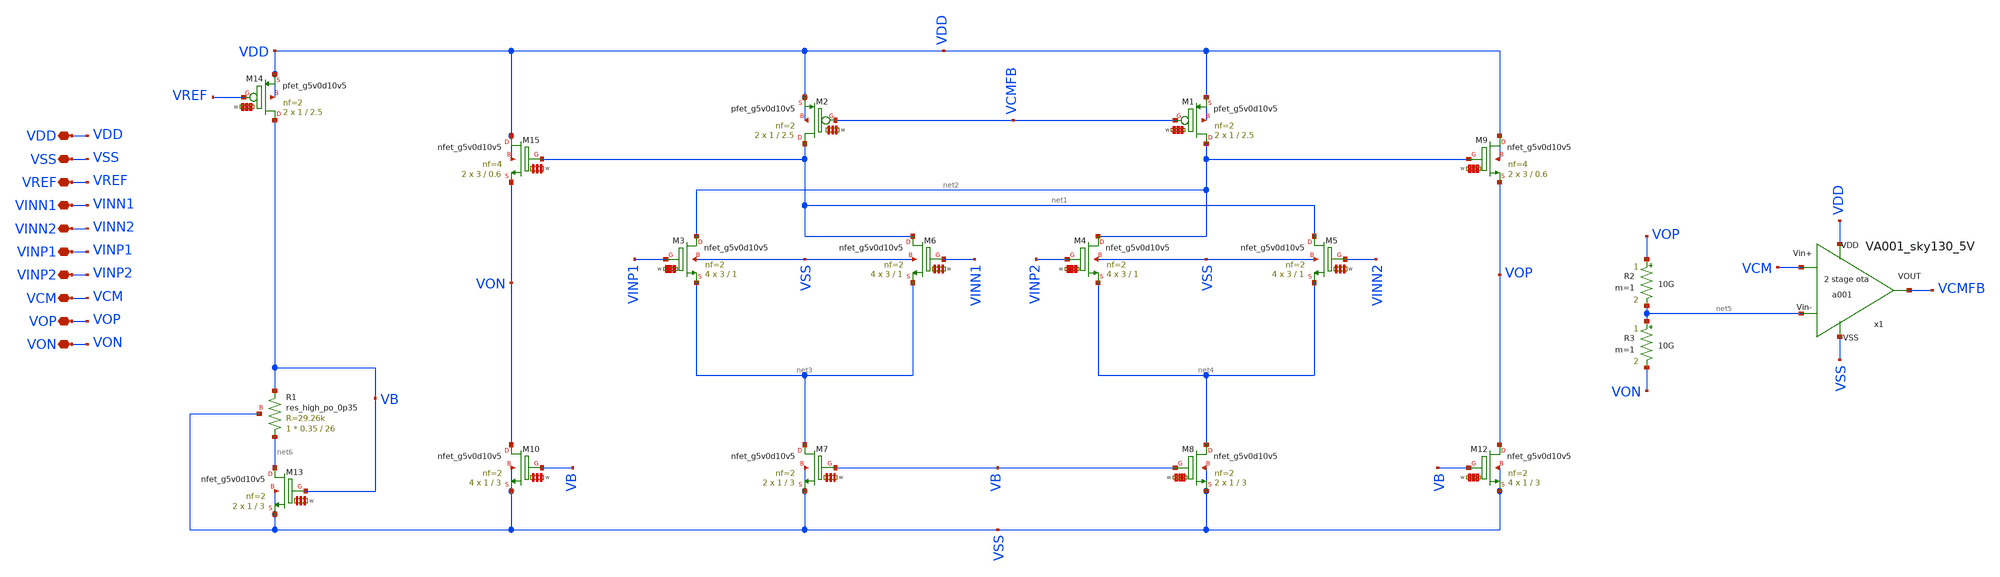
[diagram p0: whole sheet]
** sch_path: LIB/Sky130A/DDA/DDA002_NMOS_sky130_5V.sch
**.subckt DDA002_NMOS_sky130_5V VDD VSS VREF VINN1 VINN2 VINP1 VINP2 VCM VOP VON
*.iopin VDD
*.iopin VSS
*.iopin VREF
*.iopin VINN1
*.iopin VINN2
*.iopin VINP1
*.iopin VINP2
*.iopin VCM
*.iopin VOP
*.iopin VON
XM2 net1 VCMFB VDD VDD sky130_fd_pr__pfet_g5v0d10v5 L=2.5 W='1 * 2 ' nf=2 ad='int((2 + 1)/2) * 1 * 0.29'
+ as='int((2 + 2)/2) * 1 * 0.29' pd='2*int((2 + 1)/2) * (1 + 0.29)' ps='2*int((2 + 2)/2) * (1 + 0.29)'
+ nrd='0.29 / 1 / 2 ' nrs='0.29 / 1 / 2 ' sa=0 sb=0 sd=0 mult=2 m=2
XM3 net2 VINP1 net3 VSS sky130_fd_pr__nfet_g5v0d10v5 L=1 W='3 * 2 ' nf=2 ad='int((nf+1)/2) * W / nf * 0.29'
+ as='int((nf+2)/2) * W / nf * 0.29' pd='2*int((nf+1)/2) * (W / nf + 0.29)' ps='2*int((nf+2)/2) * (W / nf + 0.29)'
+ nrd='0.29 / W ' nrs='0.29 / W ' sa=0 sb=0 sd=0 mult=4 m=4
x1 VDD VSS VCM net5 VCMFB VA001_sky130_5V
R2 VOP net5 10G m=1
R3 net5 VON 10G m=1
XM13 net6 VB VSS VSS sky130_fd_pr__nfet_g5v0d10v5 L=3 W='1 * 2 ' nf=2 ad='int((nf+1)/2) * W / nf * 0.29'
+ as='int((nf+2)/2) * W / nf * 0.29' pd='2*int((nf+1)/2) * (W / nf + 0.29)' ps='2*int((nf+2)/2) * (W / nf + 0.29)'
+ nrd='0.29 / W ' nrs='0.29 / W ' sa=0 sb=0 sd=0 mult=2 m=2
XR1 net6 VB VSS sky130_fd_pr__res_high_po_0p35 L=26 mult=1 m=1
XM14 VB VREF VDD VDD sky130_fd_pr__pfet_g5v0d10v5 L=2.5 W='1 * 2 ' nf=2 ad='int((2 + 1)/2) * 1 * 0.29'
+ as='int((2 + 2)/2) * 1 * 0.29' pd='2*int((2 + 1)/2) * (1 + 0.29)' ps='2*int((2 + 2)/2) * (1 + 0.29)'
+ nrd='0.29 / 1 / 2 ' nrs='0.29 / 1 / 2 ' sa=0 sb=0 sd=0 mult=2 m=2
XM7 net3 VB VSS VSS sky130_fd_pr__nfet_g5v0d10v5 L=3 W='1 * 2 ' nf=2 ad='int((nf+1)/2) * W / nf * 0.29'
+ as='int((nf+2)/2) * W / nf * 0.29' pd='2*int((nf+1)/2) * (W / nf + 0.29)' ps='2*int((nf+2)/2) * (W / nf + 0.29)'
+ nrd='0.29 / W ' nrs='0.29 / W ' sa=0 sb=0 sd=0 mult=2 m=2
XM8 net4 VB VSS VSS sky130_fd_pr__nfet_g5v0d10v5 L=3 W='1 * 2 ' nf=2 ad='int((nf+1)/2) * W / nf * 0.29'
+ as='int((nf+2)/2) * W / nf * 0.29' pd='2*int((nf+1)/2) * (W / nf + 0.29)' ps='2*int((nf+2)/2) * (W / nf + 0.29)'
+ nrd='0.29 / W ' nrs='0.29 / W ' sa=0 sb=0 sd=0 mult=2 m=2
XM10 VON VB VSS VSS sky130_fd_pr__nfet_g5v0d10v5 L=3 W='1 * 2 ' nf=2 ad='int((nf+1)/2) * W / nf * 0.29'
+ as='int((nf+2)/2) * W / nf * 0.29' pd='2*int((nf+1)/2) * (W / nf + 0.29)' ps='2*int((nf+2)/2) * (W / nf + 0.29)'
+ nrd='0.29 / W ' nrs='0.29 / W ' sa=0 sb=0 sd=0 mult=4 m=4
XM12 VOP VB VSS VSS sky130_fd_pr__nfet_g5v0d10v5 L=3 W='1 * 2 ' nf=2 ad='int((nf+1)/2) * W / nf * 0.29'
+ as='int((nf+2)/2) * W / nf * 0.29' pd='2*int((nf+1)/2) * (W / nf + 0.29)' ps='2*int((nf+2)/2) * (W / nf + 0.29)'
+ nrd='0.29 / W ' nrs='0.29 / W ' sa=0 sb=0 sd=0 mult=4 m=4
XM6 net1 VINN1 net3 VSS sky130_fd_pr__nfet_g5v0d10v5 L=1 W='3 * 2 ' nf=2 ad='int((nf+1)/2) * W / nf * 0.29'
+ as='int((nf+2)/2) * W / nf * 0.29' pd='2*int((nf+1)/2) * (W / nf + 0.29)' ps='2*int((nf+2)/2) * (W / nf + 0.29)'
+ nrd='0.29 / W ' nrs='0.29 / W ' sa=0 sb=0 sd=0 mult=4 m=4
XM4 net2 VINP2 net4 VSS sky130_fd_pr__nfet_g5v0d10v5 L=1 W='3 * 2 ' nf=2 ad='int((nf+1)/2) * W / nf * 0.29'
+ as='int((nf+2)/2) * W / nf * 0.29' pd='2*int((nf+1)/2) * (W / nf + 0.29)' ps='2*int((nf+2)/2) * (W / nf + 0.29)'
+ nrd='0.29 / W ' nrs='0.29 / W ' sa=0 sb=0 sd=0 mult=4 m=4
XM5 net1 VINN2 net4 VSS sky130_fd_pr__nfet_g5v0d10v5 L=1 W='3 * 2 ' nf=2 ad='int((nf+1)/2) * W / nf * 0.29'
+ as='int((nf+2)/2) * W / nf * 0.29' pd='2*int((nf+1)/2) * (W / nf + 0.29)' ps='2*int((nf+2)/2) * (W / nf + 0.29)'
+ nrd='0.29 / W ' nrs='0.29 / W ' sa=0 sb=0 sd=0 mult=4 m=4
XM1 net2 VCMFB VDD VDD sky130_fd_pr__pfet_g5v0d10v5 L=2.5 W='1 * 2 ' nf=2 ad='int((2 + 1)/2) * 1 * 0.29'
+ as='int((2 + 2)/2) * 1 * 0.29' pd='2*int((2 + 1)/2) * (1 + 0.29)' ps='2*int((2 + 2)/2) * (1 + 0.29)'
+ nrd='0.29 / 1 / 2 ' nrs='0.29 / 1 / 2 ' sa=0 sb=0 sd=0 mult=2 m=2
XM15 VDD net1 VON VDD sky130_fd_pr__nfet_g5v0d10v5 L=0.6 W='3 * 4 ' nf=4 ad='int((nf+1)/2) * W / nf * 0.29'
+ as='int((nf+2)/2) * W / nf * 0.29' pd='2*int((nf+1)/2) * (W / nf + 0.29)' ps='2*int((nf+2)/2) * (W / nf + 0.29)'
+ nrd='0.29 / W ' nrs='0.29 / W ' sa=0 sb=0 sd=0 mult=2 m=2
XM9 VDD net2 VOP VDD sky130_fd_pr__nfet_g5v0d10v5 L=0.6 W='3 * 4 ' nf=4 ad='int((nf+1)/2) * W / nf * 0.29'
+ as='int((nf+2)/2) * W / nf * 0.29' pd='2*int((nf+1)/2) * (W / nf + 0.29)' ps='2*int((nf+2)/2) * (W / nf + 0.29)'
+ nrd='0.29 / W ' nrs='0.29 / W ' sa=0 sb=0 sd=0 mult=2 m=2
**.ends

* expanding   symbol:  Sky130A/single ended amplifiers/VA001_sky130_5V.sym # of pins=5
** sym_path: LIB/Sky130A/single ended amplifiers/VA001_sky130_5V.sym
** sch_path: LIB/Sky130A/single ended amplifiers/VA001_sky130_5V.sch
.subckt VA001_sky130_5V VDD VSS Vin+ Vin- VOUT
*.iopin VDD
*.iopin VSS
*.iopin Vin+
*.iopin Vin-
*.iopin VOUT
XM9 VB1 VB2 net3 VSS sky130_fd_pr__nfet_g5v0d10v5 L=2 W='1 * 2 ' nf=2 ad='int((nf+1)/2) * W / nf * 0.29'
+ as='int((nf+2)/2) * W / nf * 0.29' pd='2*int((nf+1)/2) * (W / nf + 0.29)' ps='2*int((nf+2)/2) * (W / nf + 0.29)'
+ nrd='0.29 / W ' nrs='0.29 / W ' sa=0 sb=0 sd=0 mult=2 m=2
XM10 VB2 VB2 net1 VSS sky130_fd_pr__nfet_g5v0d10v5 L=2 W='1 * 2 ' nf=2 ad='int((nf+1)/2) * W / nf * 0.29'
+ as='int((nf+2)/2) * W / nf * 0.29' pd='2*int((nf+1)/2) * (W / nf + 0.29)' ps='2*int((nf+2)/2) * (W / nf + 0.29)'
+ nrd='0.29 / W ' nrs='0.29 / W ' sa=0 sb=0 sd=0 mult=2 m=2
XM3 VB2 VB1 VDD VDD sky130_fd_pr__pfet_g5v0d10v5 L=2.5 W='1 * 2 ' nf=2 ad='int((2 + 1)/2) * 1 * 0.29'
+ as='int((2 + 2)/2) * 1 * 0.29' pd='2*int((2 + 1)/2) * (1 + 0.29)' ps='2*int((2 + 2)/2) * (1 + 0.29)'
+ nrd='0.29 / 1 / 2 ' nrs='0.29 / 1 / 2 ' sa=0 sb=0 sd=0 mult=2 m=2
XM4 VB1 VB1 VDD VDD sky130_fd_pr__pfet_g5v0d10v5 L=2.5 W='1 * 2 ' nf=2 ad='int((2 + 1)/2) * 1 * 0.29'
+ as='int((2 + 2)/2) * 1 * 0.29' pd='2*int((2 + 1)/2) * (1 + 0.29)' ps='2*int((2 + 2)/2) * (1 + 0.29)'
+ nrd='0.29 / 1 / 2 ' nrs='0.29 / 1 / 2 ' sa=0 sb=0 sd=0 mult=2 m=2
XM5 net1 net1 VSS VSS sky130_fd_pr__nfet_g5v0d10v5 L=3 W='1.2 * 2 ' nf=2 ad='int((nf+1)/2) * W / nf * 0.29'
+ as='int((nf+2)/2) * W / nf * 0.29' pd='2*int((nf+1)/2) * (W / nf + 0.29)' ps='2*int((nf+2)/2) * (W / nf + 0.29)'
+ nrd='0.29 / W ' nrs='0.29 / W ' sa=0 sb=0 sd=0 mult=2 m=2
XM6 net3 net1 net2 VSS sky130_fd_pr__nfet_g5v0d10v5 L=3 W='1.2 * 2 ' nf=2 ad='int((nf+1)/2) * W / nf * 0.29'
+ as='int((nf+2)/2) * W / nf * 0.29' pd='2*int((nf+1)/2) * (W / nf + 0.29)' ps='2*int((nf+2)/2) * (W / nf + 0.29)'
+ nrd='0.29 / W ' nrs='0.29 / W ' sa=0 sb=0 sd=0 mult=8 m=8
XR2 VSS net2 VSS sky130_fd_pr__res_high_po_0p35 L=20 mult=1 m=1
XM1 net4 VB1 VDD VDD sky130_fd_pr__pfet_g5v0d10v5 L=2.5 W='1 * 2 ' nf=2 ad='int((2 + 1)/2) * 1 * 0.29'
+ as='int((2 + 2)/2) * 1 * 0.29' pd='2*int((2 + 1)/2) * (1 + 0.29)' ps='2*int((2 + 2)/2) * (1 + 0.29)'
+ nrd='0.29 / 1 / 2 ' nrs='0.29 / 1 / 2 ' sa=0 sb=0 sd=0 mult=6 m=6
XM2 net6 Vin- net4 net4 sky130_fd_pr__pfet_g5v0d10v5 L=1 W='3 * 2 ' nf=2 ad='int((2 + 1)/2) * 3 * 0.29'
+ as='int((2 + 2)/2) * 3 * 0.29' pd='2*int((2 + 1)/2) * (3 + 0.29)' ps='2*int((2 + 2)/2) * (3 + 0.29)'
+ nrd='0.29 / 3 / 2 ' nrs='0.29 / 3 / 2 ' sa=0 sb=0 sd=0 mult=4 m=4
XM11 net6 net6 VSS VSS sky130_fd_pr__nfet_g5v0d10v5 L=2 W='1.2 * 2 ' nf=2 ad='int((nf+1)/2) * W / nf * 0.29'
+ as='int((nf+2)/2) * W / nf * 0.29' pd='2*int((nf+1)/2) * (W / nf + 0.29)' ps='2*int((nf+2)/2) * (W / nf + 0.29)'
+ nrd='0.29 / W ' nrs='0.29 / W ' sa=0 sb=0 sd=0 mult=2 m=2
XM8 net5 net6 VSS VSS sky130_fd_pr__nfet_g5v0d10v5 L=2 W='1.2 * 2 ' nf=2 ad='int((nf+1)/2) * W / nf * 0.29'
+ as='int((nf+2)/2) * W / nf * 0.29' pd='2*int((nf+1)/2) * (W / nf + 0.29)' ps='2*int((nf+2)/2) * (W / nf + 0.29)'
+ nrd='0.29 / W ' nrs='0.29 / W ' sa=0 sb=0 sd=0 mult=2 m=2
XM12 VOUT net5 VSS VSS sky130_fd_pr__nfet_g5v0d10v5 L=1 W='2 * 4 ' nf=4 ad='int((nf+1)/2) * W / nf * 0.29'
+ as='int((nf+2)/2) * W / nf * 0.29' pd='2*int((nf+1)/2) * (W / nf + 0.29)' ps='2*int((nf+2)/2) * (W / nf + 0.29)'
+ nrd='0.29 / W ' nrs='0.29 / W ' sa=0 sb=0 sd=0 mult=2 m=2
XM7 net5 Vin+ net4 net4 sky130_fd_pr__pfet_g5v0d10v5 L=1 W='3 * 2 ' nf=2 ad='int((2 + 1)/2) * 3 * 0.29'
+ as='int((2 + 2)/2) * 3 * 0.29' pd='2*int((2 + 1)/2) * (3 + 0.29)' ps='2*int((2 + 2)/2) * (3 + 0.29)'
+ nrd='0.29 / 3 / 2 ' nrs='0.29 / 3 / 2 ' sa=0 sb=0 sd=0 mult=4 m=4
XM13 VOUT VB1 VDD VDD sky130_fd_pr__pfet_g5v0d10v5 L=2.5 W='1 * 2 ' nf=2 ad='int((2 + 1)/2) * 1 * 0.29'
+ as='int((2 + 2)/2) * 1 * 0.29' pd='2*int((2 + 1)/2) * (1 + 0.29)' ps='2*int((2 + 2)/2) * (1 + 0.29)'
+ nrd='0.29 / 1 / 2 ' nrs='0.29 / 1 / 2 ' sa=0 sb=0 sd=0 mult=14 m=14
XM14 net7 VB2 net5 VSS sky130_fd_pr__nfet_g5v0d10v5 L=2.1 W='1.2 * 2 ' nf=2 ad='int((nf+1)/2) * W / nf * 0.29'
+ as='int((nf+2)/2) * W / nf * 0.29' pd='2*int((nf+1)/2) * (W / nf + 0.29)' ps='2*int((nf+2)/2) * (W / nf + 0.29)'
+ nrd='0.29 / W ' nrs='0.29 / W ' sa=0 sb=0 sd=0 mult=1 m=1
XC1 net7 VOUT sky130_fd_pr__cap_mim_m3_1 W=7.5 L=7.5 MF=4 m=4
.ends

.end
